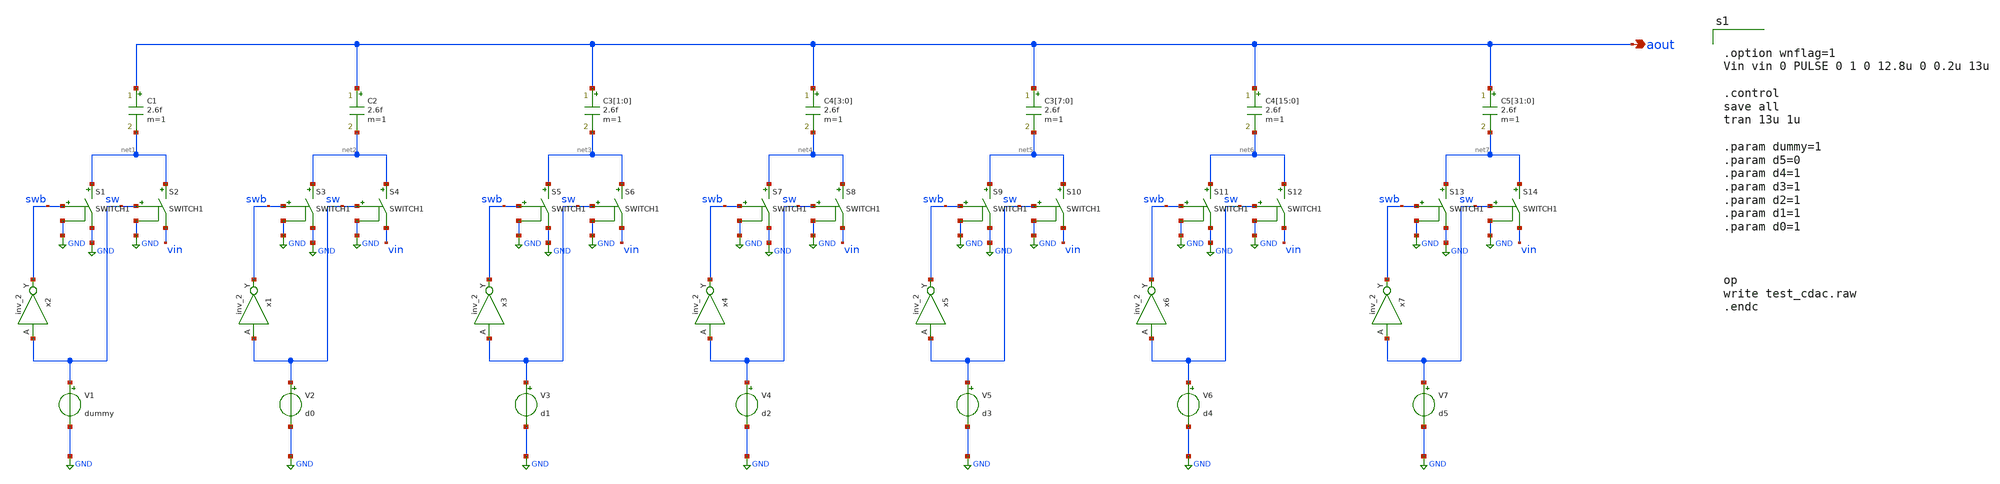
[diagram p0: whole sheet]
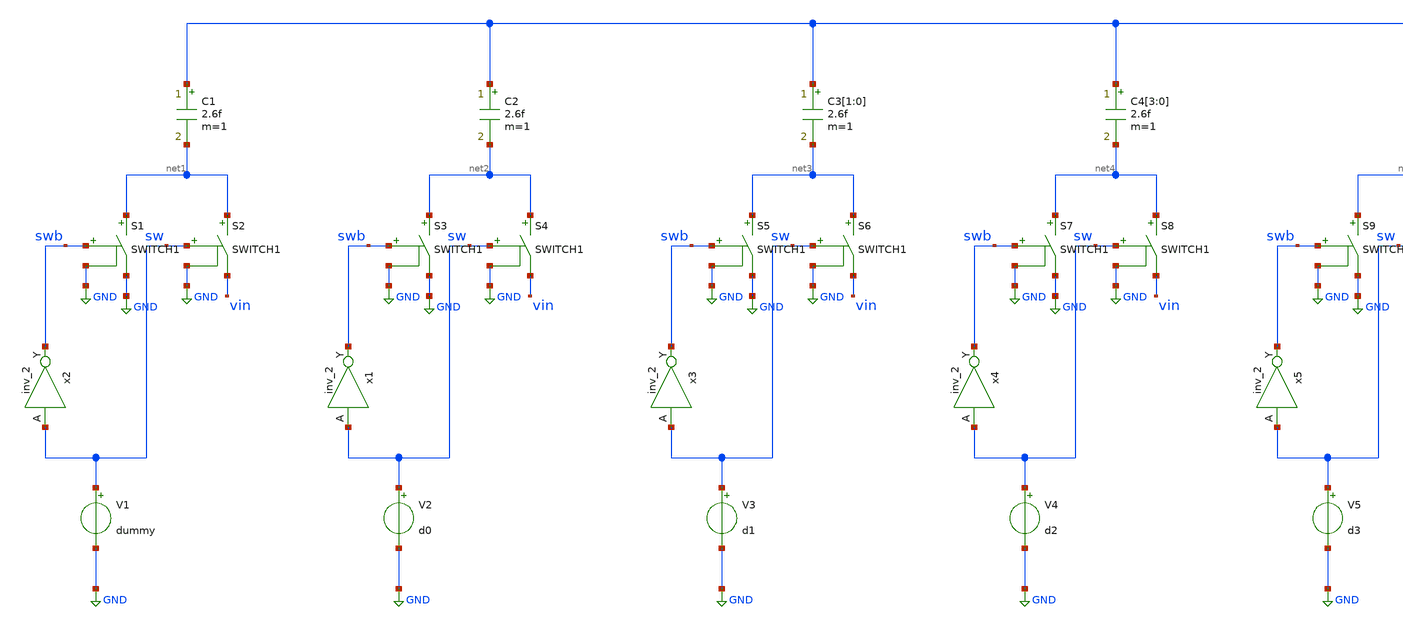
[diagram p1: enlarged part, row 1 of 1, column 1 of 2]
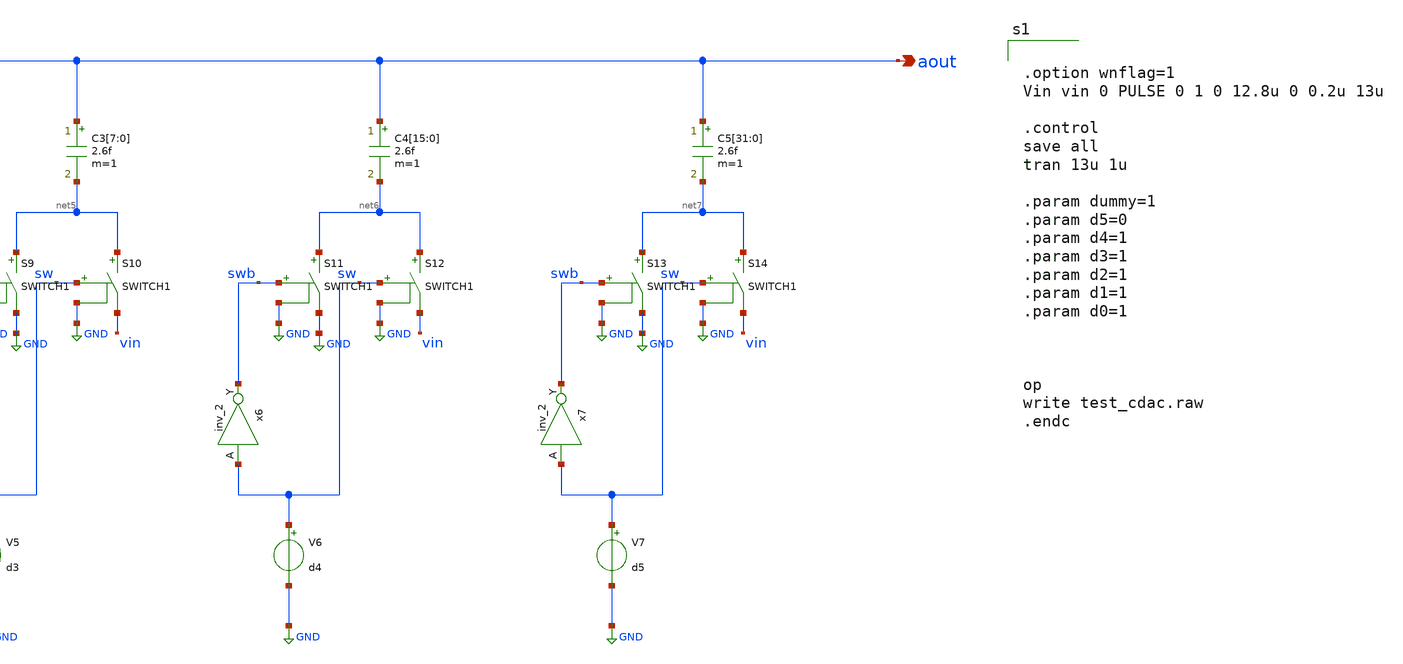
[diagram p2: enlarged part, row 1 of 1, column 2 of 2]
** sch_path: xschem/tb/cdac/tb_cdac2.sch
**.subckt tb_cdac2 aout
*.opin aout
x2 sw VGND VNB VPB VPWR swb sky130_fd_sc_hd__inv_2
V1 sw GND dummy
C1 aout net1 2.6f m=1
x1 sw VGND VNB VPB VPWR swb sky130_fd_sc_hd__inv_2
V2 sw GND d0
C2 aout net2 2.6f m=1
x3 sw VGND VNB VPB VPWR swb sky130_fd_sc_hd__inv_2
V3 sw GND d1
C3[1] aout net3 2.6f m=1
C3[0] aout net3 2.6f m=1
x4 sw VGND VNB VPB VPWR swb sky130_fd_sc_hd__inv_2
V4 sw GND d2
C4[3] aout net4 2.6f m=1
C4[2] aout net4 2.6f m=1
C4[1] aout net4 2.6f m=1
C4[0] aout net4 2.6f m=1
x5 sw VGND VNB VPB VPWR swb sky130_fd_sc_hd__inv_2
V5 sw GND d3
C3[7] aout net5 2.6f m=1
C3[6] aout net5 2.6f m=1
C3[5] aout net5 2.6f m=1
C3[4] aout net5 2.6f m=1
C3[3] aout net5 2.6f m=1
C3[2] aout net5 2.6f m=1
C3[1] aout net5 2.6f m=1
C3[0] aout net5 2.6f m=1
x6 sw VGND VNB VPB VPWR swb sky130_fd_sc_hd__inv_2
V6 sw GND d4
C4[15] aout net6 2.6f m=1
C4[14] aout net6 2.6f m=1
C4[13] aout net6 2.6f m=1
C4[12] aout net6 2.6f m=1
C4[11] aout net6 2.6f m=1
C4[10] aout net6 2.6f m=1
C4[9] aout net6 2.6f m=1
C4[8] aout net6 2.6f m=1
C4[7] aout net6 2.6f m=1
C4[6] aout net6 2.6f m=1
C4[5] aout net6 2.6f m=1
C4[4] aout net6 2.6f m=1
C4[3] aout net6 2.6f m=1
C4[2] aout net6 2.6f m=1
C4[1] aout net6 2.6f m=1
C4[0] aout net6 2.6f m=1
x7 sw VGND VNB VPB VPWR swb sky130_fd_sc_hd__inv_2
V7 sw GND d5
C5[31] aout net7 2.6f m=1
C5[30] aout net7 2.6f m=1
C5[29] aout net7 2.6f m=1
C5[28] aout net7 2.6f m=1
C5[27] aout net7 2.6f m=1
C5[26] aout net7 2.6f m=1
C5[25] aout net7 2.6f m=1
C5[24] aout net7 2.6f m=1
C5[23] aout net7 2.6f m=1
C5[22] aout net7 2.6f m=1
C5[21] aout net7 2.6f m=1
C5[20] aout net7 2.6f m=1
C5[19] aout net7 2.6f m=1
C5[18] aout net7 2.6f m=1
C5[17] aout net7 2.6f m=1
C5[16] aout net7 2.6f m=1
C5[15] aout net7 2.6f m=1
C5[14] aout net7 2.6f m=1
C5[13] aout net7 2.6f m=1
C5[12] aout net7 2.6f m=1
C5[11] aout net7 2.6f m=1
C5[10] aout net7 2.6f m=1
C5[9] aout net7 2.6f m=1
C5[8] aout net7 2.6f m=1
C5[7] aout net7 2.6f m=1
C5[6] aout net7 2.6f m=1
C5[5] aout net7 2.6f m=1
C5[4] aout net7 2.6f m=1
C5[3] aout net7 2.6f m=1
C5[2] aout net7 2.6f m=1
C5[1] aout net7 2.6f m=1
C5[0] aout net7 2.6f m=1
S1 net1 GND swb GND SWITCH1
S2 net1 vin sw GND SWITCH1
S3 net2 GND swb GND SWITCH1
S4 net2 vin sw GND SWITCH1
S5 net3 GND swb GND SWITCH1
S6 net3 vin sw GND SWITCH1
S7 net4 GND swb GND SWITCH1
S8 net4 vin sw GND SWITCH1
S9 net5 GND swb GND SWITCH1
S10 net5 vin sw GND SWITCH1
S11 net6 GND swb GND SWITCH1
S12 net6 vin sw GND SWITCH1
S13 net7 GND swb GND SWITCH1
S14 net7 vin sw GND SWITCH1
**** begin user architecture code
 * FET CORNERS
.include $::SKYWATER_MODELS/models/corners/tt.spice
*.include $::SKYWATER_MODELS//corners/ff.spice
*.include $::SKYWATER_MODELS/corners/ss.spice
*.include $::SKYWATER_MODELS/corners/sf.spice
*.include $::SKYWATER_MODELS/corners/fs.spice

* TT + R + C
*.include $::SKYWATER_MODELS/corners/tt_rmax_cmax.spice
*.include $::SKYWATER_MODELS/corners/tt_rmin_cmin.spice
*.include $::SKYWATER_MODELS/corners/tt_rmax_cmin.spice
*.include $::SKYWATER_MODELS/corners/tt_rmin_cmax.spice

* FF + R + C
*.include $::SKYWATER_MODELS/corners/ff_rmax_cmax.spice
*.include $::SKYWATER_MODELS/corners/ff_rmin_cmin.spice
*.include $::SKYWATER_MODELS/corners/ff_rmax_cmin.spice
*.include $::SKYWATER_MODELS/corners/ff_rmin_cmax.spice


* SS + R + C
*.include $::SKYWATER_MODELS/corners/ss_rmax_cmax.spice
*.include $::SKYWATER_MODELS/corners/ss_rmin_cmin.spice
*.include $::SKYWATER_MODELS/corners/ss_rmax_cmin.spice
*.include $::SKYWATER_MODELS/corners/ss_rmin_cmax.spice

* SF + R + C
*.include $::SKYWATER_MODELS/corners/sf_rmax_cmax.spice
*.include $::SKYWATER_MODELS/corners/sf_rmin_cmin.spice
*.include $::SKYWATER_MODELS/corners/sf_rmax_cmin.spice
*.include $::SKYWATER_MODELS/corners/sf_rmin_cmax.spice

* FS + R + C
*.include $::SKYWATER_MODELS/corners/fs_rmax_cmax.spice
*.include $::SKYWATER_MODELS/corners/fs_rmin_cmin.spice
*.include $::SKYWATER_MODELS/corners/fs_rmax_cmin.spice
*.include $::SKYWATER_MODELS/corners/fs_rmin_cmax.spice



.option wnflag=1
Vin vin 0 PULSE 0 1 0 12.8u 0 0.2u 13u

.control
save all
tran 13u 1u

.param dummy=1
.param d5=0
.param d4=1
.param d3=1
.param d2=1
.param d1=1
.param d0=1



op
write test_cdac.raw
.endc




.include $::SKYWATER_STDCELLS/cells/inv/sky130_fd_sc_hd__inv_2.spice
**** end user architecture code
**.ends
.GLOBAL GND
.end
